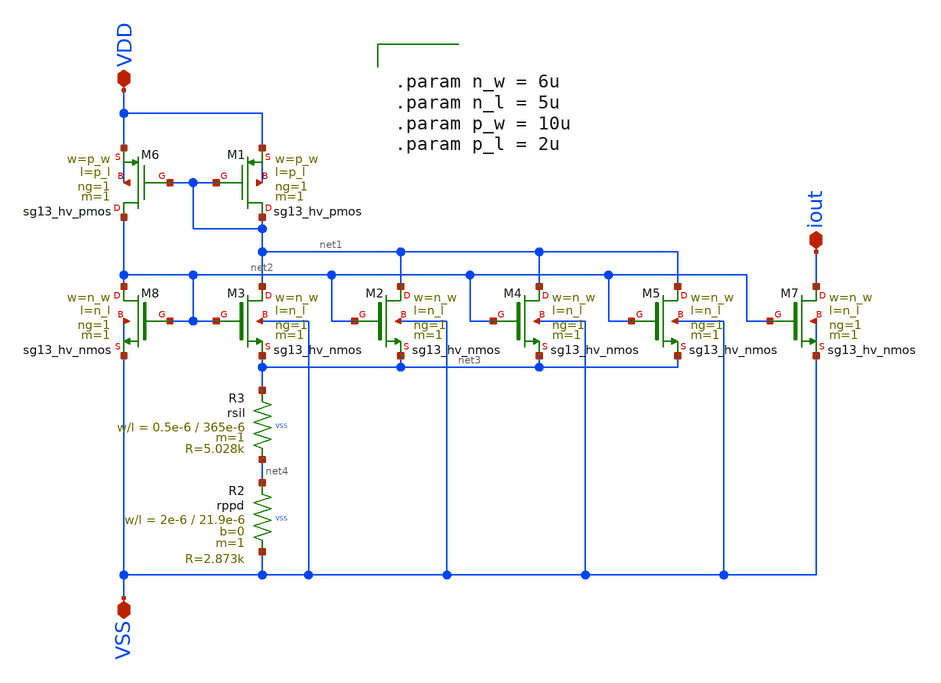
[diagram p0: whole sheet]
** sch_path: macros/heichips26_vcr/macros/switched_capacitor/schematic/xschem/current_reference_40uA.sch
**.subckt current_reference_40uA VSS VDD iout
*.iopin VSS
*.iopin VDD
*.iopin iout
XM8 net2 net2 VSS VSS sg13_hv_nmos w=n_w l=n_l ng=1 m=1 mm_ok=1
XM6 net2 net1 VDD VDD sg13_hv_pmos w=p_w l=p_l ng=1 m=1 mm_ok=1
XM1 net1 net1 VDD VDD sg13_hv_pmos w=p_w l=p_l ng=1 m=1 mm_ok=1
XM3 net1 net2 net3 VSS sg13_hv_nmos w=n_w l=n_l ng=1 m=1 mm_ok=1
XR2 net4 VSS VSS rppd w=2e-6 l=21.9e-6 m=1 b=0 mm_ok=1
XM2 net1 net2 net3 VSS sg13_hv_nmos w=n_w l=n_l ng=1 m=1 mm_ok=1
XM4 net1 net2 net3 VSS sg13_hv_nmos w=n_w l=n_l ng=1 m=1 mm_ok=1
XM5 net1 net2 net3 VSS sg13_hv_nmos w=n_w l=n_l ng=1 m=1 mm_ok=1
XM7 iout net2 VSS VSS sg13_hv_nmos w=n_w l=n_l ng=1 m=1 mm_ok=1
XR3 net3 net4 VSS rsil w=0.5e-6 l=365e-6 m=1 mm_ok=1
**** begin user architecture code


.param n_w = 6u
.param n_l = 5u
.param p_w = 10u
.param p_l = 2u


**** end user architecture code
**.ends
.end
